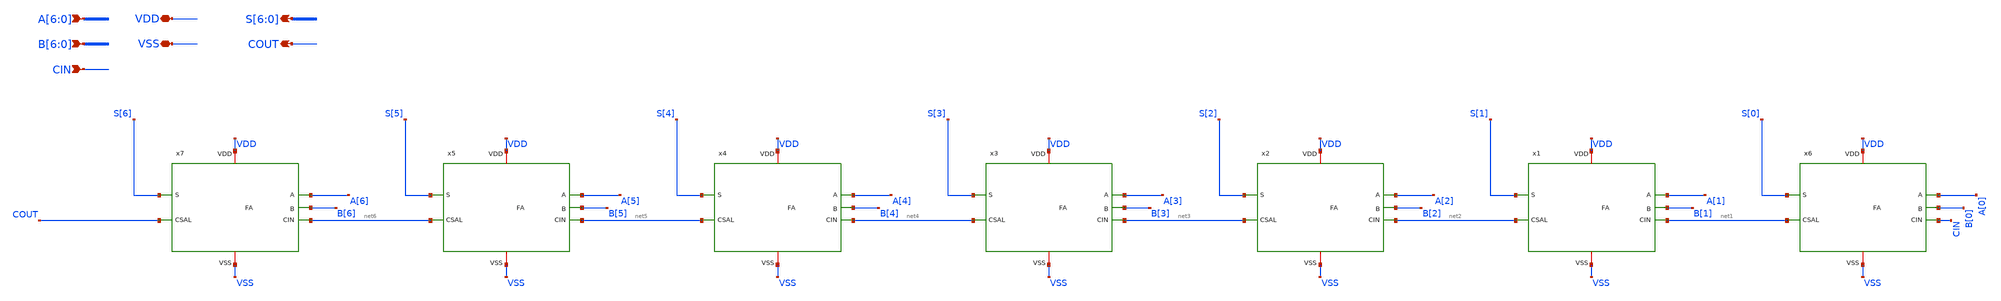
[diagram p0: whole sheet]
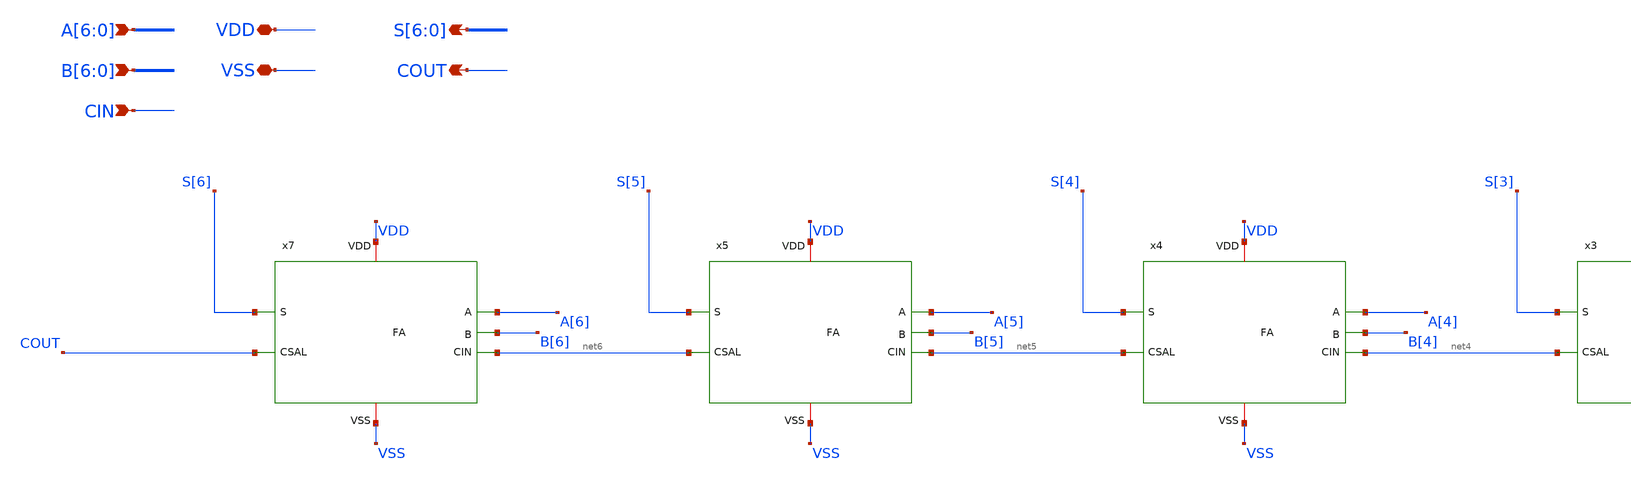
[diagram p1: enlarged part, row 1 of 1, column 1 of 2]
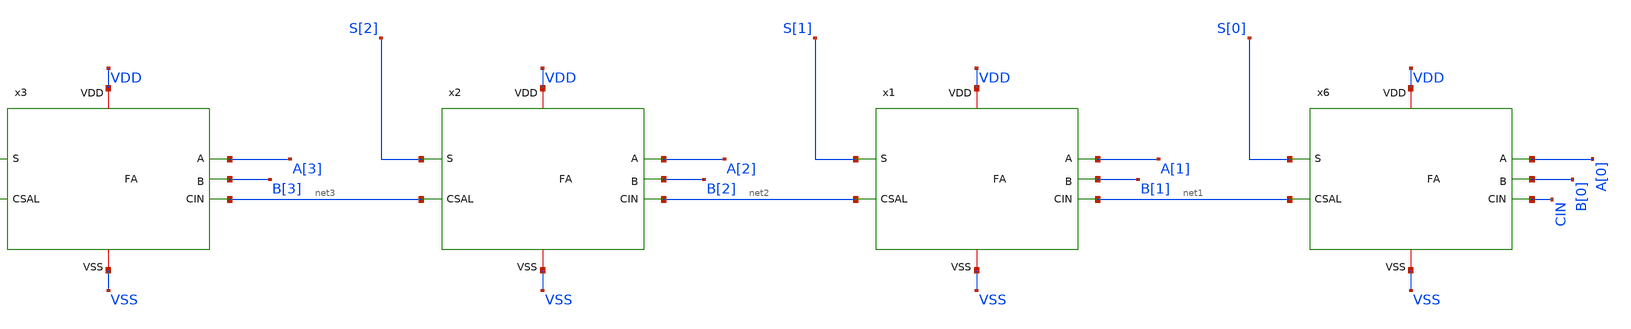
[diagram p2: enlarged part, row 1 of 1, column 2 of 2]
** sch_path: 27_03_26/TOP_MAXI/Esquematicos/Counter_FA_7bits.sch
**.subckt Counter_FA_7bits VDD VSS A[6],A[5],A[4],A[3],A[2],A[1],A[0]
*+ B[6],B[5],B[4],B[3],B[2],B[1],B[0] CIN S[6],S[5],S[4],S[3],S[2],S[1],S[0] COUT
*.iopin VDD
*.iopin VSS
*.ipin A[6],A[5],A[4],A[3],A[2],A[1],A[0]
*.ipin B[6],B[5],B[4],B[3],B[2],B[1],B[0]
*.ipin CIN
*.opin S[6],S[5],S[4],S[3],S[2],S[1],S[0]
*.opin COUT
x6 A[0] VDD B[0] S[0] VSS CIN net1 FA
x1 A[1] VDD B[1] S[1] VSS net1 net2 FA
x2 A[2] VDD B[2] S[2] VSS net2 net3 FA
x3 A[3] VDD B[3] S[3] VSS net3 net4 FA
x4 A[4] VDD B[4] S[4] VSS net4 net5 FA
x5 A[5] VDD B[5] S[5] VSS net5 net6 FA
x7 A[6] VDD B[6] S[6] VSS net6 COUT FA
**.ends
.end
